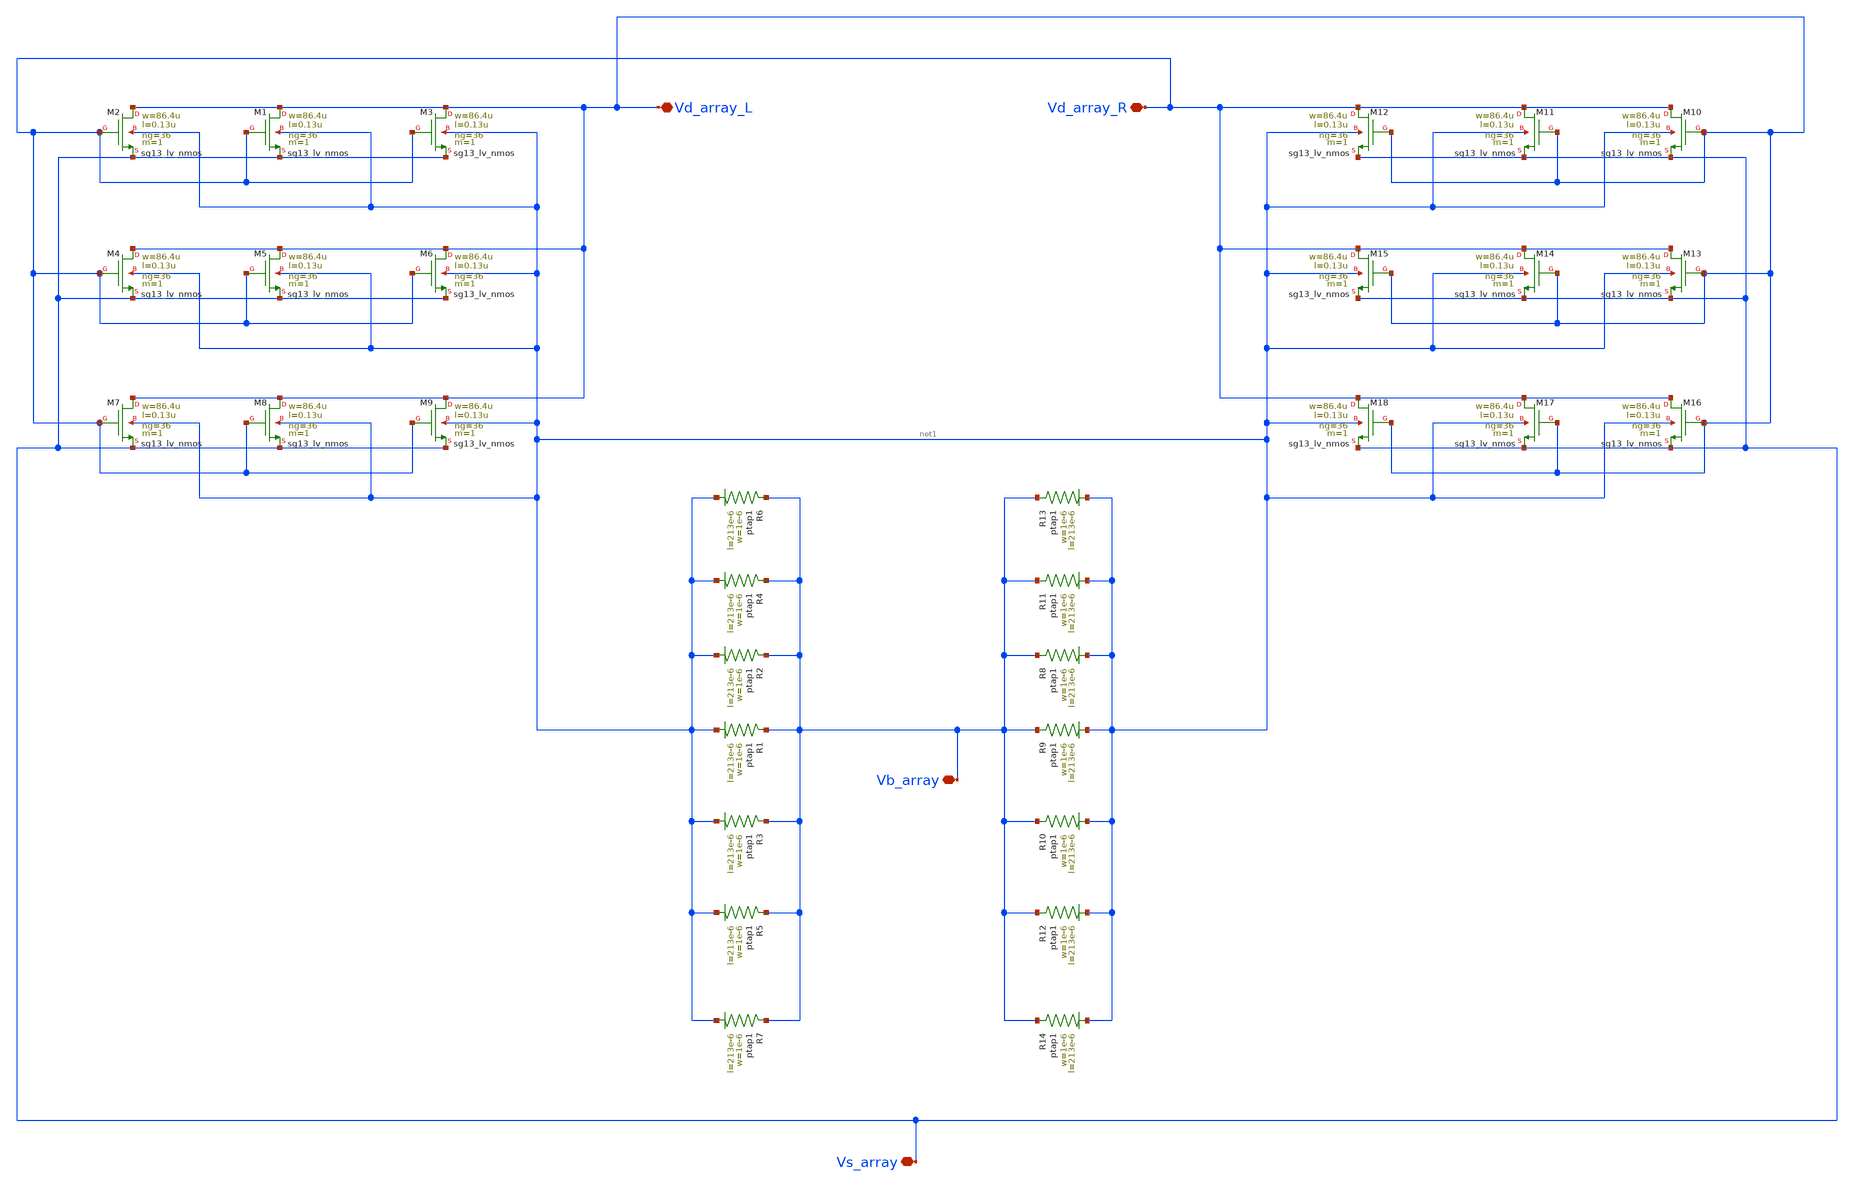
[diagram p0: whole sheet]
** sch_path: Layouts/PMOS/nmos_array_x2.sch
**.subckt nmos_array_x2 Vd_array_L Vs_array Vd_array_R Vb_array
*.iopin Vd_array_L
*.iopin Vs_array
*.iopin Vd_array_R
*.iopin Vb_array
XM2 Vd_array_L Vd_array_R Vs_array net1 sg13_lv_nmos w=86.4u l=0.13u ng=36 m=1 mm_ok=1
XR2 Vb_array net1 ptap1 R=1.529 w=1e-6 l=213e-6
XM1 Vd_array_L Vd_array_R Vs_array net1 sg13_lv_nmos w=86.4u l=0.13u ng=36 m=1 mm_ok=1
XM3 Vd_array_L Vd_array_R Vs_array net1 sg13_lv_nmos w=86.4u l=0.13u ng=36 m=1 mm_ok=1
XM4 Vd_array_L Vd_array_R Vs_array net1 sg13_lv_nmos w=86.4u l=0.13u ng=36 m=1 mm_ok=1
XM5 Vd_array_L Vd_array_R Vs_array net1 sg13_lv_nmos w=86.4u l=0.13u ng=36 m=1 mm_ok=1
XM6 Vd_array_L Vd_array_R Vs_array net1 sg13_lv_nmos w=86.4u l=0.13u ng=36 m=1 mm_ok=1
XM7 Vd_array_L Vd_array_R Vs_array net1 sg13_lv_nmos w=86.4u l=0.13u ng=36 m=1 mm_ok=1
XM8 Vd_array_L Vd_array_R Vs_array net1 sg13_lv_nmos w=86.4u l=0.13u ng=36 m=1 mm_ok=1
XM9 Vd_array_L Vd_array_R Vs_array net1 sg13_lv_nmos w=86.4u l=0.13u ng=36 m=1 mm_ok=1
XR1 Vb_array net1 ptap1 R=1.529 w=1e-6 l=213e-6
XR3 Vb_array net1 ptap1 R=1.529 w=1e-6 l=213e-6
XR4 Vb_array net1 ptap1 R=1.529 w=1e-6 l=213e-6
XR5 Vb_array net1 ptap1 R=1.529 w=1e-6 l=213e-6
XR6 Vb_array net1 ptap1 R=1.529 w=1e-6 l=213e-6
XR7 Vb_array net1 ptap1 R=1.529 w=1e-6 l=213e-6
XM10 Vd_array_R Vd_array_L Vs_array net1 sg13_lv_nmos w=86.4u l=0.13u ng=36 m=1 mm_ok=1
XR8 Vb_array net1 ptap1 R=1.529 w=1e-6 l=213e-6
XM11 Vd_array_R Vd_array_L Vs_array net1 sg13_lv_nmos w=86.4u l=0.13u ng=36 m=1 mm_ok=1
XM12 Vd_array_R Vd_array_L Vs_array net1 sg13_lv_nmos w=86.4u l=0.13u ng=36 m=1 mm_ok=1
XM13 Vd_array_R Vd_array_L Vs_array net1 sg13_lv_nmos w=86.4u l=0.13u ng=36 m=1 mm_ok=1
XM14 Vd_array_R Vd_array_L Vs_array net1 sg13_lv_nmos w=86.4u l=0.13u ng=36 m=1 mm_ok=1
XM15 Vd_array_R Vd_array_L Vs_array net1 sg13_lv_nmos w=86.4u l=0.13u ng=36 m=1 mm_ok=1
XM16 Vd_array_R Vd_array_L Vs_array net1 sg13_lv_nmos w=86.4u l=0.13u ng=36 m=1 mm_ok=1
XM17 Vd_array_R Vd_array_L Vs_array net1 sg13_lv_nmos w=86.4u l=0.13u ng=36 m=1 mm_ok=1
XM18 Vd_array_R Vd_array_L Vs_array net1 sg13_lv_nmos w=86.4u l=0.13u ng=36 m=1 mm_ok=1
XR9 Vb_array net1 ptap1 R=1.529 w=1e-6 l=213e-6
XR10 Vb_array net1 ptap1 R=1.529 w=1e-6 l=213e-6
XR11 Vb_array net1 ptap1 R=1.529 w=1e-6 l=213e-6
XR12 Vb_array net1 ptap1 R=1.529 w=1e-6 l=213e-6
XR13 Vb_array net1 ptap1 R=1.529 w=1e-6 l=213e-6
XR14 Vb_array net1 ptap1 R=1.529 w=1e-6 l=213e-6
**.ends
.end
